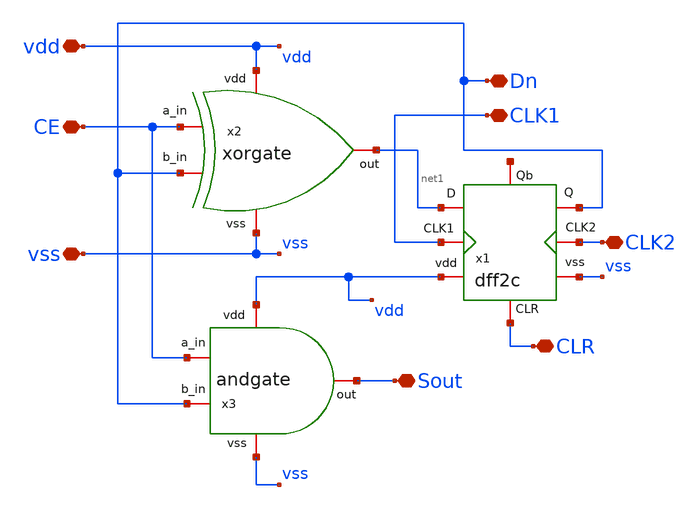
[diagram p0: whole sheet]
** sch_path: design/blocks/count1bit_2c/schematic/count1bit_2c.sch
**.subckt count1bit_2c Dn CLK1 CLR Sout vss CE vdd CLK2
*.iopin Dn
*.iopin CLK1
*.iopin CLR
*.iopin Sout
*.iopin vss
*.iopin CE
*.iopin vdd
*.iopin CLK2
x2 vdd net1 vss CE Dn xorgate
x3 vdd CE Sout Dn vss andgate
x1 net1 Dn CLR vdd net2 CLK1 CLK2 vss dff2c
**.ends
.end
